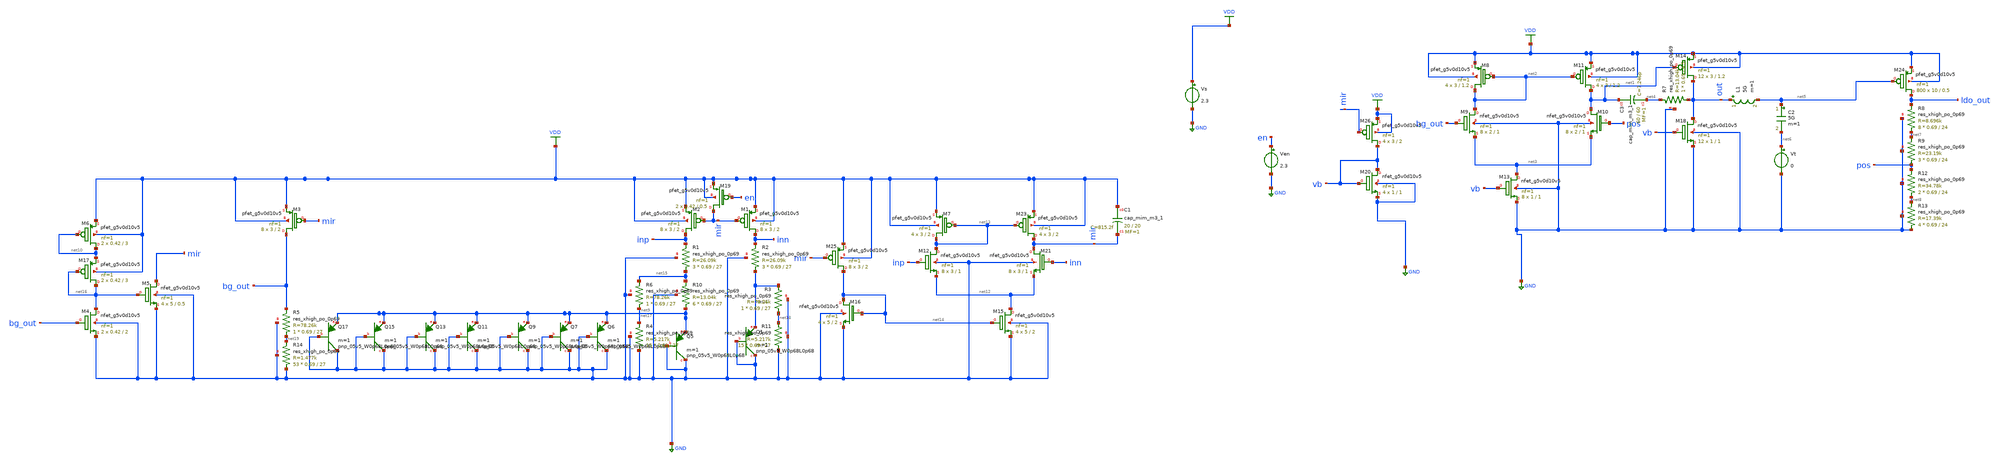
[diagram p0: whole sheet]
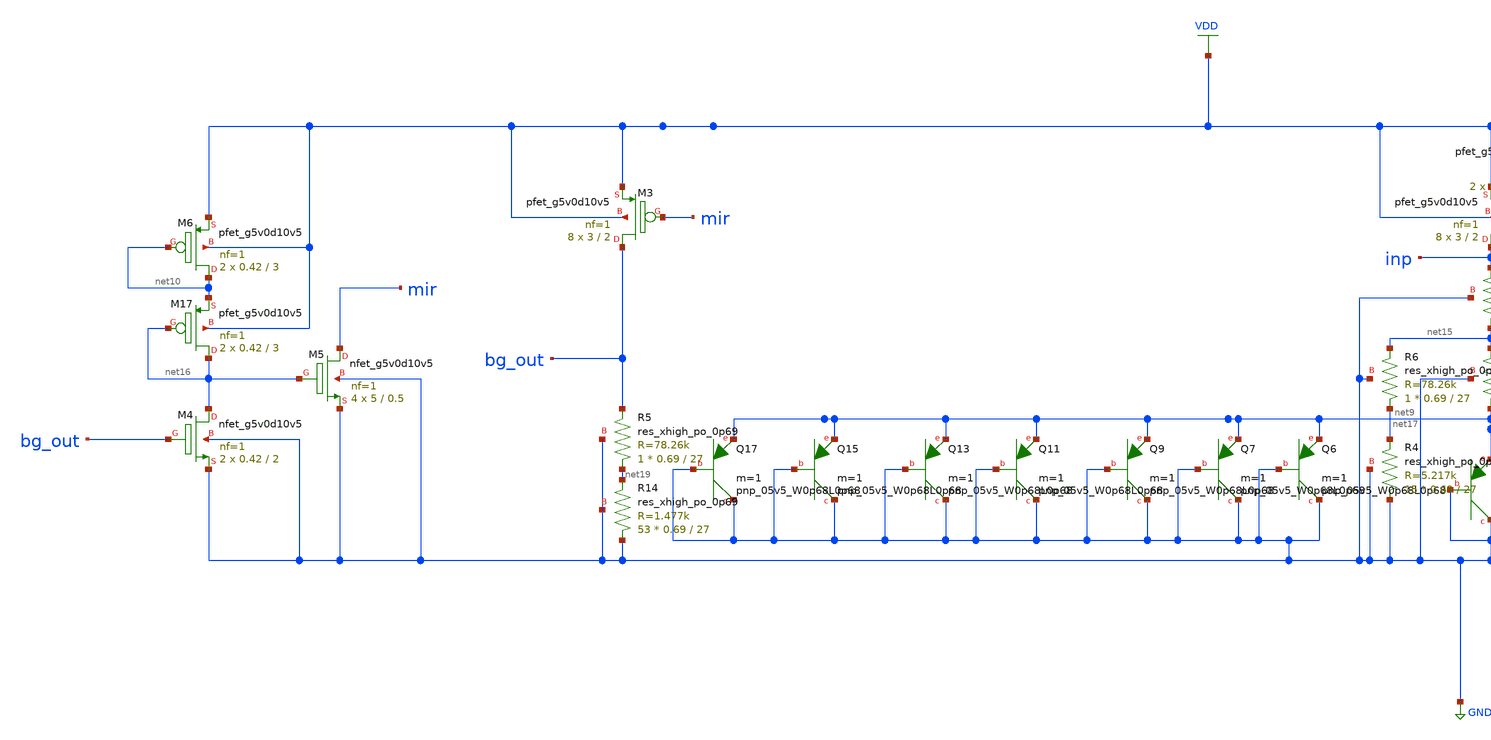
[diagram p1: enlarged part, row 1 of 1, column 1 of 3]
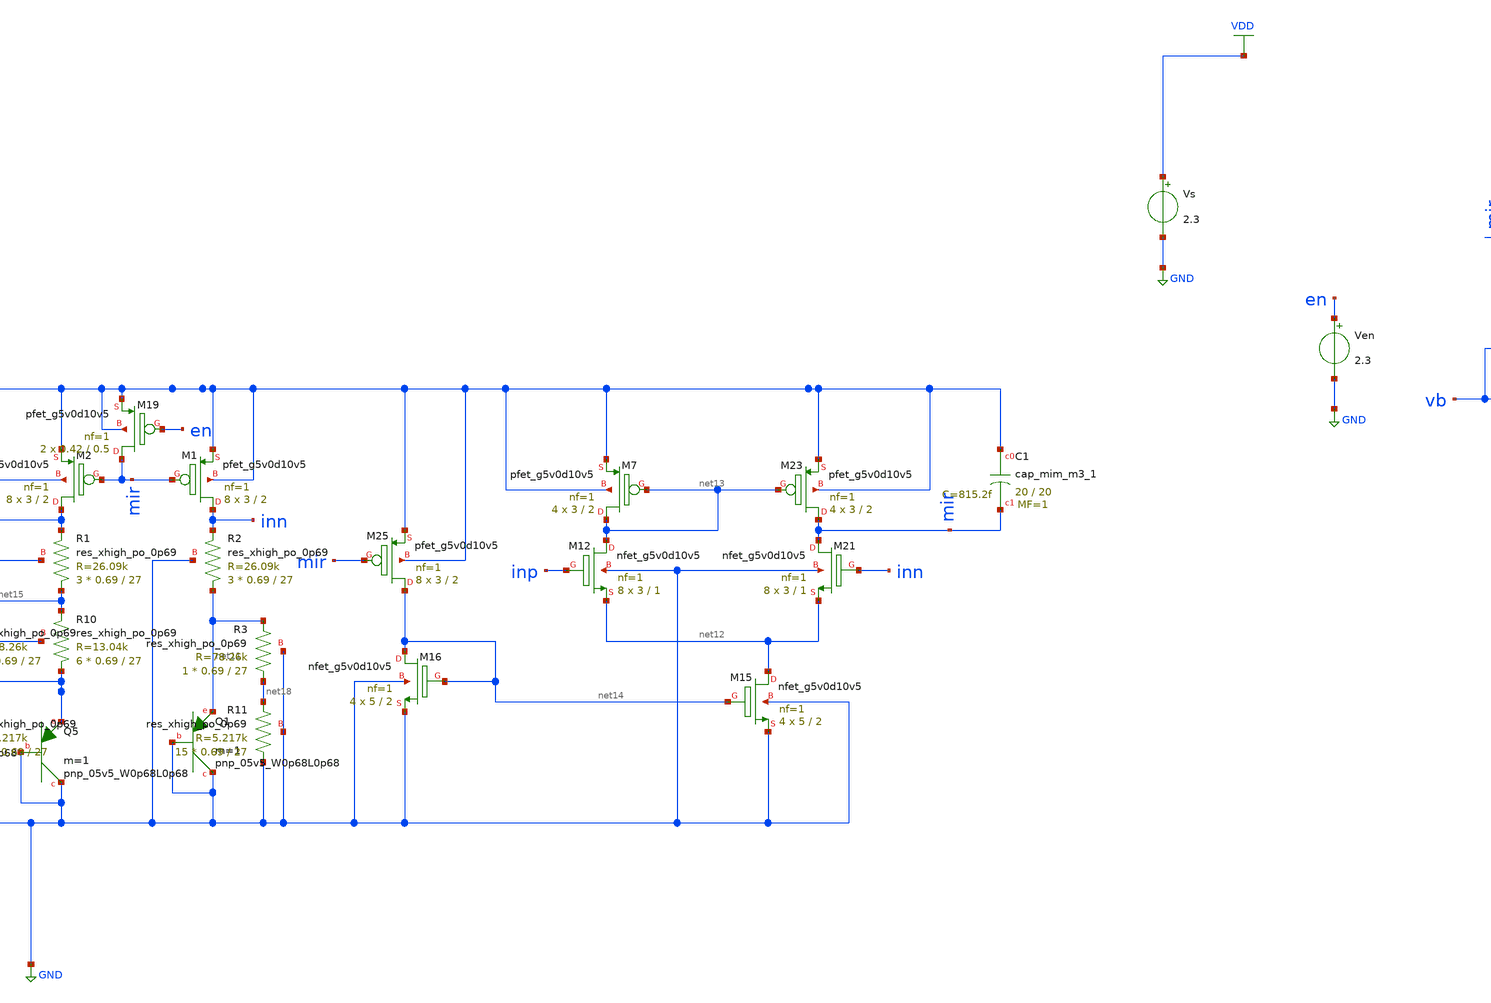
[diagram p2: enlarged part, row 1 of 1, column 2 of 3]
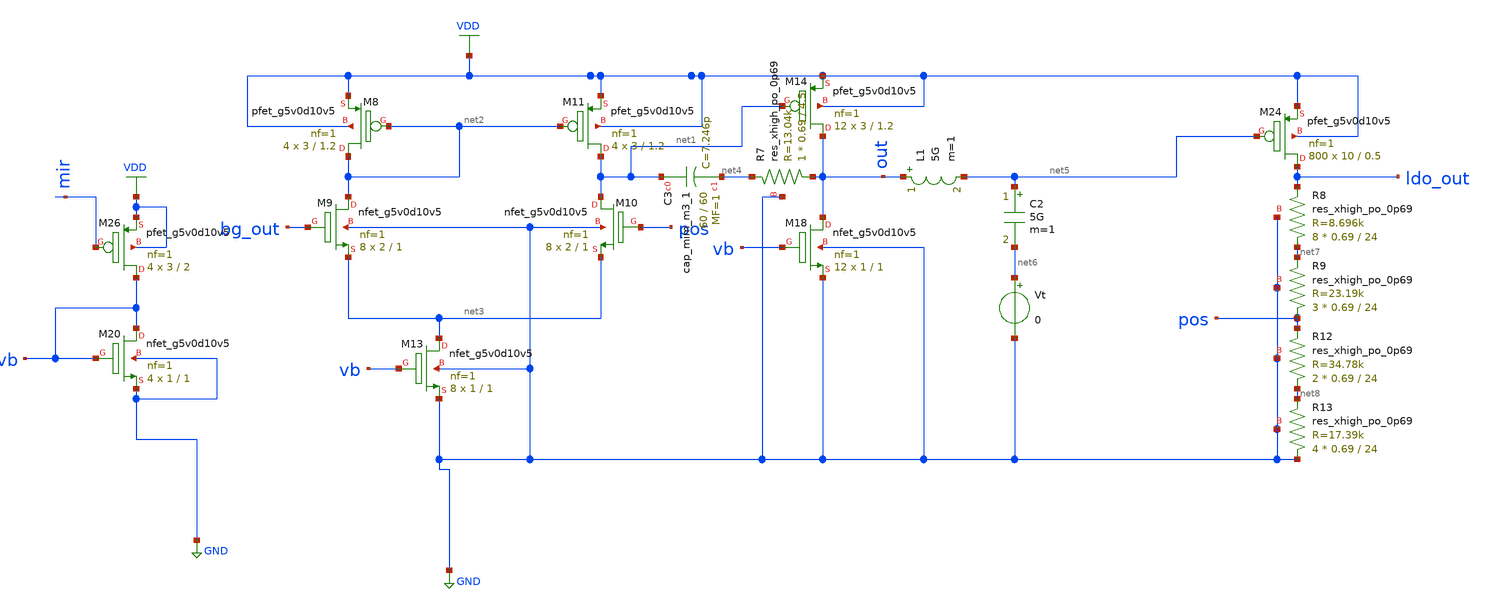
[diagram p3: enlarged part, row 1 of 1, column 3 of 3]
** sch_path: xschem/untitled-17.sch
**.subckt untitled-17
XM8 net2 net2 VDD VDD sky130_fd_pr__pfet_g5v0d10v5 L=1.2 W=3 nf=1 ad='int((nf+1)/2) * W/nf * 0.29' as='int((nf+2)/2) * W/nf * 0.29'
+ pd='2*int((nf+1)/2) * (W/nf + 0.29)' ps='2*int((nf+2)/2) * (W/nf + 0.29)' nrd='0.29 / W' nrs='0.29 / W'
+ sa=0 sb=0 sd=0 mult=4 m=4
XM9 net2 bg_out net3 GND sky130_fd_pr__nfet_g5v0d10v5 L=1 W=2 nf=1 ad='int((nf+1)/2) * W/nf * 0.29' as='int((nf+2)/2) * W/nf * 0.29'
+ pd='2*int((nf+1)/2) * (W/nf + 0.29)' ps='2*int((nf+2)/2) * (W/nf + 0.29)' nrd='0.29 / W' nrs='0.29 / W'
+ sa=0 sb=0 sd=0 mult=8 m=8
XM10 net1 pos net3 GND sky130_fd_pr__nfet_g5v0d10v5 L=1 W=2 nf=1 ad='int((nf+1)/2) * W/nf * 0.29' as='int((nf+2)/2) * W/nf * 0.29'
+ pd='2*int((nf+1)/2) * (W/nf + 0.29)' ps='2*int((nf+2)/2) * (W/nf + 0.29)' nrd='0.29 / W' nrs='0.29 / W'
+ sa=0 sb=0 sd=0 mult=8 m=8
XM11 net1 net2 VDD VDD sky130_fd_pr__pfet_g5v0d10v5 L=1.2 W=3 nf=1 ad='int((nf+1)/2) * W/nf * 0.29' as='int((nf+2)/2) * W/nf * 0.29'
+ pd='2*int((nf+1)/2) * (W/nf + 0.29)' ps='2*int((nf+2)/2) * (W/nf + 0.29)' nrd='0.29 / W' nrs='0.29 / W'
+ sa=0 sb=0 sd=0 mult=4 m=4
XM13 net3 vb GND GND sky130_fd_pr__nfet_g5v0d10v5 L=1 W=1 nf=1 ad='int((nf+1)/2) * W/nf * 0.29' as='int((nf+2)/2) * W/nf * 0.29'
+ pd='2*int((nf+1)/2) * (W/nf + 0.29)' ps='2*int((nf+2)/2) * (W/nf + 0.29)' nrd='0.29 / W' nrs='0.29 / W'
+ sa=0 sb=0 sd=0 mult=8 m=8
XM14 out net1 VDD VDD sky130_fd_pr__pfet_g5v0d10v5 L=1.2 W=3 nf=1 ad='int((nf+1)/2) * W/nf * 0.29' as='int((nf+2)/2) * W/nf * 0.29'
+ pd='2*int((nf+1)/2) * (W/nf + 0.29)' ps='2*int((nf+2)/2) * (W/nf + 0.29)' nrd='0.29 / W' nrs='0.29 / W'
+ sa=0 sb=0 sd=0 mult=12 m=12
XM18 out vb GND GND sky130_fd_pr__nfet_g5v0d10v5 L=1 W=1 nf=1 ad='int((nf+1)/2) * W/nf * 0.29' as='int((nf+2)/2) * W/nf * 0.29'
+ pd='2*int((nf+1)/2) * (W/nf + 0.29)' ps='2*int((nf+2)/2) * (W/nf + 0.29)' nrd='0.29 / W' nrs='0.29 / W'
+ sa=0 sb=0 sd=0 mult=12 m=12
XM20 vb vb GND GND sky130_fd_pr__nfet_g5v0d10v5 L=1 W=1 nf=1 ad='int((nf+1)/2) * W/nf * 0.29' as='int((nf+2)/2) * W/nf * 0.29'
+ pd='2*int((nf+1)/2) * (W/nf + 0.29)' ps='2*int((nf+2)/2) * (W/nf + 0.29)' nrd='0.29 / W' nrs='0.29 / W'
+ sa=0 sb=0 sd=0 mult=4 m=4
XM24 ldo_out net5 VDD VDD sky130_fd_pr__pfet_g5v0d10v5 L=0.5 W=10 nf=1 ad='int((nf+1)/2) * W/nf * 0.29'
+ as='int((nf+2)/2) * W/nf * 0.29' pd='2*int((nf+1)/2) * (W/nf + 0.29)' ps='2*int((nf+2)/2) * (W/nf + 0.29)'
+ nrd='0.29 / W' nrs='0.29 / W' sa=0 sb=0 sd=0 mult=800 m=800
XM26 vb mir VDD VDD sky130_fd_pr__pfet_g5v0d10v5 L=2 W=3 nf=1 ad='int((nf+1)/2) * W/nf * 0.29' as='int((nf+2)/2) * W/nf * 0.29'
+ pd='2*int((nf+1)/2) * (W/nf + 0.29)' ps='2*int((nf+2)/2) * (W/nf + 0.29)' nrd='0.29 / W' nrs='0.29 / W'
+ sa=0 sb=0 sd=0 mult=4 m=4
XC3 net1 net4 sky130_fd_pr__cap_mim_m3_1 W=60 L=60 MF=1 m=1
XR7 out net4 GND sky130_fd_pr__res_xhigh_po_0p69 L=4.5 mult=1 m=1
Vs VDD GND 2.3
Vt net6 GND 0
C2 net5 net6 5G m=1
L1 out net5 5G m=1
XR8 net7 ldo_out GND sky130_fd_pr__res_xhigh_po_0p69 L=24 mult=8 m=8
XR9 pos net7 GND sky130_fd_pr__res_xhigh_po_0p69 L=24 mult=3 m=3
XR12 net8 pos GND sky130_fd_pr__res_xhigh_po_0p69 L=24 mult=2 m=2
XR13 GND net8 GND sky130_fd_pr__res_xhigh_po_0p69 L=24 mult=4 m=4
XM1 inn mir VDD VDD sky130_fd_pr__pfet_g5v0d10v5 L=2 W=3 nf=1 ad='int((nf+1)/2) * W/nf * 0.29' as='int((nf+2)/2) * W/nf * 0.29'
+ pd='2*int((nf+1)/2) * (W/nf + 0.29)' ps='2*int((nf+2)/2) * (W/nf + 0.29)' nrd='0.29 / W' nrs='0.29 / W'
+ sa=0 sb=0 sd=0 mult=8 m=8
XM2 inp mir VDD VDD sky130_fd_pr__pfet_g5v0d10v5 L=2 W=3 nf=1 ad='int((nf+1)/2) * W/nf * 0.29' as='int((nf+2)/2) * W/nf * 0.29'
+ pd='2*int((nf+1)/2) * (W/nf + 0.29)' ps='2*int((nf+2)/2) * (W/nf + 0.29)' nrd='0.29 / W' nrs='0.29 / W'
+ sa=0 sb=0 sd=0 mult=8 m=8
XM3 bg_out mir VDD VDD sky130_fd_pr__pfet_g5v0d10v5 L=2 W=3 nf=1 ad='int((nf+1)/2) * W/nf * 0.29' as='int((nf+2)/2) * W/nf * 0.29'
+ pd='2*int((nf+1)/2) * (W/nf + 0.29)' ps='2*int((nf+2)/2) * (W/nf + 0.29)' nrd='0.29 / W' nrs='0.29 / W'
+ sa=0 sb=0 sd=0 mult=8 m=8
XQ1 GND GND net11 sky130_fd_pr__pnp_05v5_W0p68L0p68 m=1
XQ5 GND GND net9 sky130_fd_pr__pnp_05v5_W0p68L0p68 m=1
XQ6 GND GND net9 sky130_fd_pr__pnp_05v5_W0p68L0p68 m=1
XQ7 GND GND net9 sky130_fd_pr__pnp_05v5_W0p68L0p68 m=1
XQ9 GND GND net9 sky130_fd_pr__pnp_05v5_W0p68L0p68 m=1
XQ11 GND GND net9 sky130_fd_pr__pnp_05v5_W0p68L0p68 m=1
XQ13 GND GND net9 sky130_fd_pr__pnp_05v5_W0p68L0p68 m=1
XQ15 GND GND net9 sky130_fd_pr__pnp_05v5_W0p68L0p68 m=1
XQ17 GND GND net9 sky130_fd_pr__pnp_05v5_W0p68L0p68 m=1
XM4 net16 bg_out GND GND sky130_fd_pr__nfet_g5v0d10v5 L=2 W=0.42 nf=1 ad='int((nf+1)/2) * W/nf * 0.29'
+ as='int((nf+2)/2) * W/nf * 0.29' pd='2*int((nf+1)/2) * (W/nf + 0.29)' ps='2*int((nf+2)/2) * (W/nf + 0.29)'
+ nrd='0.29 / W' nrs='0.29 / W' sa=0 sb=0 sd=0 mult=2 m=2
XM5 mir net16 GND GND sky130_fd_pr__nfet_g5v0d10v5 L=0.5 W=5 nf=1 ad='int((nf+1)/2) * W/nf * 0.29' as='int((nf+2)/2) * W/nf * 0.29'
+ pd='2*int((nf+1)/2) * (W/nf + 0.29)' ps='2*int((nf+2)/2) * (W/nf + 0.29)' nrd='0.29 / W' nrs='0.29 / W'
+ sa=0 sb=0 sd=0 mult=4 m=4
XM6 net10 net10 VDD VDD sky130_fd_pr__pfet_g5v0d10v5 L=3 W=0.42 nf=1 ad='int((nf+1)/2) * W/nf * 0.29'
+ as='int((nf+2)/2) * W/nf * 0.29' pd='2*int((nf+1)/2) * (W/nf + 0.29)' ps='2*int((nf+2)/2) * (W/nf + 0.29)'
+ nrd='0.29 / W' nrs='0.29 / W' sa=0 sb=0 sd=0 mult=2 m=2
XM7 net13 net13 VDD VDD sky130_fd_pr__pfet_g5v0d10v5 L=2 W=3 nf=1 ad='int((nf+1)/2) * W/nf * 0.29' as='int((nf+2)/2) * W/nf * 0.29'
+ pd='2*int((nf+1)/2) * (W/nf + 0.29)' ps='2*int((nf+2)/2) * (W/nf + 0.29)' nrd='0.29 / W' nrs='0.29 / W'
+ sa=0 sb=0 sd=0 mult=4 m=4
XM12 net13 inp net12 GND sky130_fd_pr__nfet_g5v0d10v5 L=1 W=3 nf=1 ad='int((nf+1)/2) * W/nf * 0.29' as='int((nf+2)/2) * W/nf * 0.29'
+ pd='2*int((nf+1)/2) * (W/nf + 0.29)' ps='2*int((nf+2)/2) * (W/nf + 0.29)' nrd='0.29 / W' nrs='0.29 / W'
+ sa=0 sb=0 sd=0 mult=8 m=8
XM21 mir inn net12 GND sky130_fd_pr__nfet_g5v0d10v5 L=1 W=3 nf=1 ad='int((nf+1)/2) * W/nf * 0.29' as='int((nf+2)/2) * W/nf * 0.29'
+ pd='2*int((nf+1)/2) * (W/nf + 0.29)' ps='2*int((nf+2)/2) * (W/nf + 0.29)' nrd='0.29 / W' nrs='0.29 / W'
+ sa=0 sb=0 sd=0 mult=8 m=8
XM23 mir net13 VDD VDD sky130_fd_pr__pfet_g5v0d10v5 L=2 W=3 nf=1 ad='int((nf+1)/2) * W/nf * 0.29' as='int((nf+2)/2) * W/nf * 0.29'
+ pd='2*int((nf+1)/2) * (W/nf + 0.29)' ps='2*int((nf+2)/2) * (W/nf + 0.29)' nrd='0.29 / W' nrs='0.29 / W'
+ sa=0 sb=0 sd=0 mult=4 m=4
XM15 net12 net14 GND GND sky130_fd_pr__nfet_g5v0d10v5 L=2 W=5 nf=1 ad='int((nf+1)/2) * W/nf * 0.29' as='int((nf+2)/2) * W/nf * 0.29'
+ pd='2*int((nf+1)/2) * (W/nf + 0.29)' ps='2*int((nf+2)/2) * (W/nf + 0.29)' nrd='0.29 / W' nrs='0.29 / W'
+ sa=0 sb=0 sd=0 mult=4 m=4
XM25 net14 mir VDD VDD sky130_fd_pr__pfet_g5v0d10v5 L=2 W=3 nf=1 ad='int((nf+1)/2) * W/nf * 0.29' as='int((nf+2)/2) * W/nf * 0.29'
+ pd='2*int((nf+1)/2) * (W/nf + 0.29)' ps='2*int((nf+2)/2) * (W/nf + 0.29)' nrd='0.29 / W' nrs='0.29 / W'
+ sa=0 sb=0 sd=0 mult=8 m=8
XM16 net14 net14 GND GND sky130_fd_pr__nfet_g5v0d10v5 L=2 W=5 nf=1 ad='int((nf+1)/2) * W/nf * 0.29' as='int((nf+2)/2) * W/nf * 0.29'
+ pd='2*int((nf+1)/2) * (W/nf + 0.29)' ps='2*int((nf+2)/2) * (W/nf + 0.29)' nrd='0.29 / W' nrs='0.29 / W'
+ sa=0 sb=0 sd=0 mult=4 m=4
XC1 VDD mir sky130_fd_pr__cap_mim_m3_1 W=20 L=20 MF=1 m=1
XR1 net15 inp GND sky130_fd_pr__res_xhigh_po_0p69 L=27 mult=3 m=3
XR2 net11 inn GND sky130_fd_pr__res_xhigh_po_0p69 L=27 mult=3 m=3
XR3 net18 net11 GND sky130_fd_pr__res_xhigh_po_0p69 L=27 mult=1 m=1
XR10 net9 net15 GND sky130_fd_pr__res_xhigh_po_0p69 L=27 mult=6 m=6
XR4 GND net17 GND sky130_fd_pr__res_xhigh_po_0p69 L=27 mult=15 m=15
XR11 GND net18 GND sky130_fd_pr__res_xhigh_po_0p69 L=27 mult=15 m=15
XR6 net17 net15 GND sky130_fd_pr__res_xhigh_po_0p69 L=27 mult=1 m=1
XR5 net19 bg_out GND sky130_fd_pr__res_xhigh_po_0p69 L=27 mult=1 m=1
XR14 GND net19 GND sky130_fd_pr__res_xhigh_po_0p69 L=27 mult=53 m=53
XM19 mir en VDD VDD sky130_fd_pr__pfet_g5v0d10v5 L=0.5 W=0.42 nf=1 ad='int((nf+1)/2) * W/nf * 0.29' as='int((nf+2)/2) * W/nf * 0.29'
+ pd='2*int((nf+1)/2) * (W/nf + 0.29)' ps='2*int((nf+2)/2) * (W/nf + 0.29)' nrd='0.29 / W' nrs='0.29 / W'
+ sa=0 sb=0 sd=0 mult=2 m=2
Ven en GND 2.3
XM17 net16 net16 net10 VDD sky130_fd_pr__pfet_g5v0d10v5 L=3 W=0.42 nf=1 ad='int((nf+1)/2) * W/nf * 0.29'
+ as='int((nf+2)/2) * W/nf * 0.29' pd='2*int((nf+1)/2) * (W/nf + 0.29)' ps='2*int((nf+2)/2) * (W/nf + 0.29)'
+ nrd='0.29 / W' nrs='0.29 / W' sa=0 sb=0 sd=0 mult=2 m=2
**** begin user architecture code


.param R=18k
R10 ldo_out GND {R}
IL ldo_out 0 PWL(0 0.1m 10u 0.1m 20u 10m 30u 10m)
*CL ldo_out gnd 10p
.lib /home/mustafa/mabrains/pdks/share/pdk/sky130A/libs.tech/ngspice/sky130.lib_mod.spice tt




.nodeset v(inn)=1.2
.nodeset v(inp)=1.2
.nodeset v(mir)=1
.nodeset v(net13)=1
.nodeset v(bg_out)=1.1
.nodeset v(ldo_out)=1.8
.nodeset v(pos)=1.1
*.nodeset v(net3)=0.8
*.nodeset v(net1)=0.7
.nodeset v(net14)=0.9
*.nodeset v(net7)=0.75
.nodeset v(vb)=0.9

.option temp=27
*User_defined_functions
.control
define max(vector_name) (vecmax(vector_name))
define min(vector_name) (vecmin(vector_name))
.endc


*Temp_sweep
.control
alter IL 0
dc temp 85 0 -1
let temp_coeff=1000000*(max(ldo_out)-min(ldo_out))/85
print temp_coeff
plot v(ldo_out)
set wr_singlescale
set wr_vecnames
set appendwrite
.endc


.control
alter IL 0
*alter R10 1G
op
let iq =i(Vs)
print iq
*print all
set wr_singlescale
set wr_vecnames
set appendwrite
if v(ldo_out)>1
wrdata op_point_test v(ldo_out)
end
.endc



*Stability_Analysis
.control
alter IL 0
alter Vs AC =0
alter Vt AC=1
ac dec 10 1 1G
plot vdb(out)
plot (180/pi)*vp(out)
let ph= (180/pi)*vp(out)
meas ac pm FIND ph WHEN vdb(out)=0
.endc


*PSRR_Analysis
.control
alter IL 0
alter Vs AC =1
alter Vt AC=0
alter L1 0
alter C2 0
ac dec 10 1 1G
meas AC PSRR100 FIND vdb(ldo_out) AT=100
meas AC PSRR100k FIND vdb(ldo_out) AT=100k
plot vdb(ldo_out)
.endc




*supply_sweep
.control
alter IL 0
dc Vs 2.8 0 -0.01
plot vdd ldo_out
meas DC Vldo_Sup_2 FIND ldo_out AT=2
meas DC Vldo_nom FIND ldo_out AT=2.3
meas DC Vldo_Sup_2_8 FIND ldo_out AT=2.8
let line_reg = abs((Vldo_Sup_2_8-Vldo_Sup_2)/0.8)
print line_reg
meas DC vin WHEN v(ldo_out)=1.764
let dropout=vin-1.764
print dropout
set wr_singlescale
set wr_vecnames
set appendwrite
.endc





*Load_Reg_switches
*V1 c1 0 DC 0 PWL(0 5 20u 5 35u 0 50u 0 100u 0)
*V2 c2 0 DC 0 PWL(0 0 20u 0 35u 0 50u 5 100u 5)
*s1 ldo_out 2 c1 0 switch1 ON
*s2 ldo_out 3 c2 0 switch1 OFF
*.model switch1 sw vt=0.1 ron =0.1 roff =1G
*R1 2 0 18k
*R2 3 0 180

*.control
*alter R10 1G
*tran 0.1u 90u
*plot v(ldo_out) v(c1) v(c2)
*meas TRAN V_ldo_100u FIND v(ldo_out) AT=10u
*meas TRAN V_ldo_10m FIND v(ldo_out) AT=50u
*let load_reg= V_ldo_100u-V_ldo_10m
*print load_reg
*.endc


**Load_Transient
.control
alter IL 50u
alter R10 3600k
tran 0.1u 100u
meas TRAN V_ldo_100u FIND v(ldo_out) AT=5u
meas TRAN V_ldo_10m FIND v(ldo_out) AT=100u
let load_reg= V_ldo_100u-V_ldo_10m
let load_current =(-1*i(Vs)-131.8e-6)
print load_reg
plot load_current v(ldo_out)-1.8
.endc


**Transient
.control
alter R10 36k
alter @IL[PWL] = [ 0 0 10u 0 20u 0 30u 0 ]
alter @Vs[pulse] = [ 1.8 3 10u 10u 1u 100u 200u ]
alter IL 0
tran 0.1u 100u
plot vdd ldo_out
.endc
.control
alter R10 36k
alter @IL[PWL] = [ 0 0 10u 0 20u 0 30u 0 ]
alter @Vs[pulse] = [ 0 2.3 10u 0.1u 1u 100u 200u ]
tran 0.1u 100u
plot vdd ldo_out
.endc
.control
alter R10 36k
alter @IL[PWL] = [ 0 0 10u 0 20u 0 30u 0 ]
alter @Ven[pulse] = [ 0 2.3 10u 0.1u 1u 100u 200u ]
tran 0.1u 100u
*meas TRAN st_up_time when v(ldo_out)>1.782
plot en ldo_out
.endc






**** end user architecture code
**.ends
.GLOBAL GND
.GLOBAL VDD
.end
